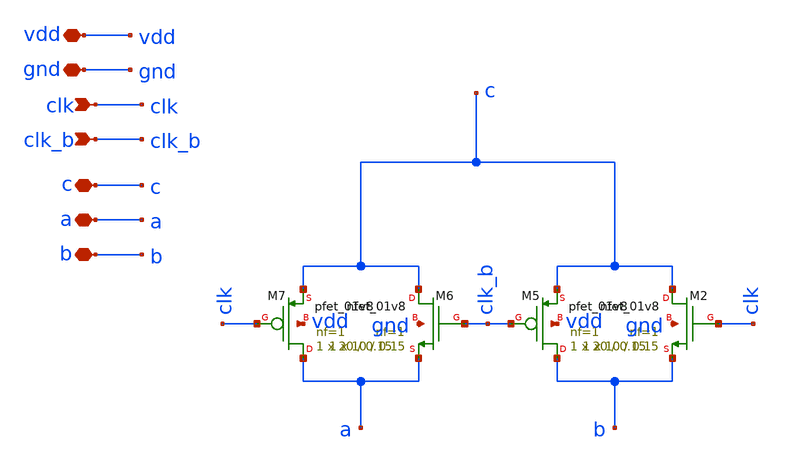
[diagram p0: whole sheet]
** sch_path: xschem/dac/dac_sw.sch
**.subckt dac_sw vdd gnd clk clk_b c a b
*.iopin vdd
*.iopin gnd
*.ipin clk
*.ipin clk_b
*.iopin c
*.iopin a
*.iopin b
XM2 c clk b gnd sky130_fd_pr__nfet_01v8 L=0.15 W=10 nf=1 ad='int((nf+1)/2) * W/nf * 0.29' as='int((nf+2)/2) * W/nf * 0.29'
+ pd='2*int((nf+1)/2) * (W/nf + 0.29)' ps='2*int((nf+2)/2) * (W/nf + 0.29)' nrd='0.29 / W' nrs='0.29 / W'
+ sa=0 sb=0 sd=0 mult=1 m=1
XM5 b clk_b c vdd sky130_fd_pr__pfet_01v8 L=0.15 W=20 nf=1 ad='int((nf+1)/2) * W/nf * 0.29' as='int((nf+2)/2) * W/nf * 0.29'
+ pd='2*int((nf+1)/2) * (W/nf + 0.29)' ps='2*int((nf+2)/2) * (W/nf + 0.29)' nrd='0.29 / W' nrs='0.29 / W'
+ sa=0 sb=0 sd=0 mult=1 m=1
XM6 c clk_b a gnd sky130_fd_pr__nfet_01v8 L=0.15 W=10 nf=1 ad='int((nf+1)/2) * W/nf * 0.29' as='int((nf+2)/2) * W/nf * 0.29'
+ pd='2*int((nf+1)/2) * (W/nf + 0.29)' ps='2*int((nf+2)/2) * (W/nf + 0.29)' nrd='0.29 / W' nrs='0.29 / W'
+ sa=0 sb=0 sd=0 mult=1 m=1
XM7 a clk c vdd sky130_fd_pr__pfet_01v8 L=0.15 W=20 nf=1 ad='int((nf+1)/2) * W/nf * 0.29' as='int((nf+2)/2) * W/nf * 0.29'
+ pd='2*int((nf+1)/2) * (W/nf + 0.29)' ps='2*int((nf+2)/2) * (W/nf + 0.29)' nrd='0.29 / W' nrs='0.29 / W'
+ sa=0 sb=0 sd=0 mult=1 m=1
**.ends
.end
